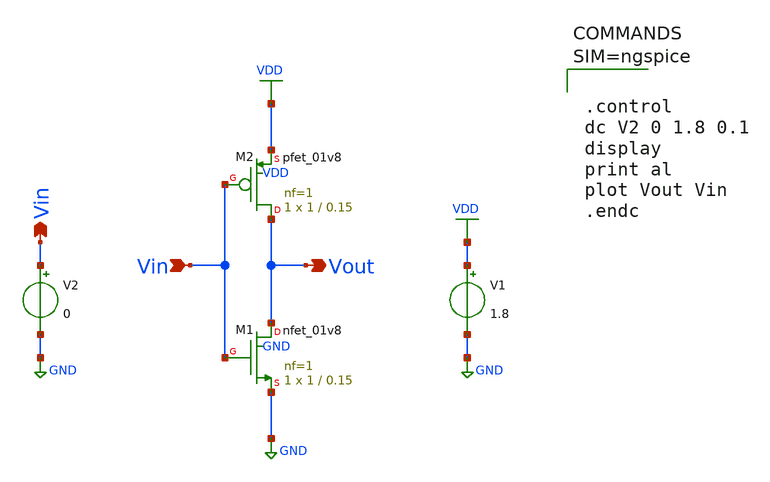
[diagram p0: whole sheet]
** sch_path: Ngspice/Inverter/Load_Characteristics/Inverter_Load_Characteristics.sch
**.subckt Inverter_Load_Characteristics Vin Vin Vout
*.opin Vin
*.ipin Vin
*.opin Vout
V1 VDD GND 1.8
XM1 Vout Vin GND GND sky130_fd_pr__nfet_01v8 L=0.15 W=1 nf=1 ad='int((1 + 1)/2) * 1 / 1 * 0.29' as='int((1 + 2)/2) * 1 / 1 * 0.29'
+ pd='2*int((1 + 1)/2) * (1 / 1 + 0.29)' ps='2*int((1 + 2)/2) * (1 / 1 + 0.29)' nrd='0.29 / 1 ' nrs='0.29 / 1 '
+ sa=0 sb=0 sd=0 mult=1 m=1
XM2 Vout Vin VDD VDD sky130_fd_pr__pfet_01v8 L=0.15 W=1 nf=1 ad='int((1 + 1)/2) * 1 / 1 * 0.29' as='int((1 + 2)/2) * 1 / 1 * 0.29'
+ pd='2*int((1 + 1)/2) * (1 / 1 + 0.29)' ps='2*int((1 + 2)/2) * (1 / 1 + 0.29)' nrd='0.29 / 1 ' nrs='0.29 / 1 '
+ sa=0 sb=0 sd=0 mult=1 m=1
V2 Vin GND 0
**** begin user architecture code

** opencircuitdesign pdks install
.lib $::SKYWATER_MODELS/sky130.lib.spice tt




.control
dc V2 0 1.8 0.1
display
print al
plot Vout Vin
.endc



**** end user architecture code
**.ends
.GLOBAL GND
.GLOBAL VDD
.end
